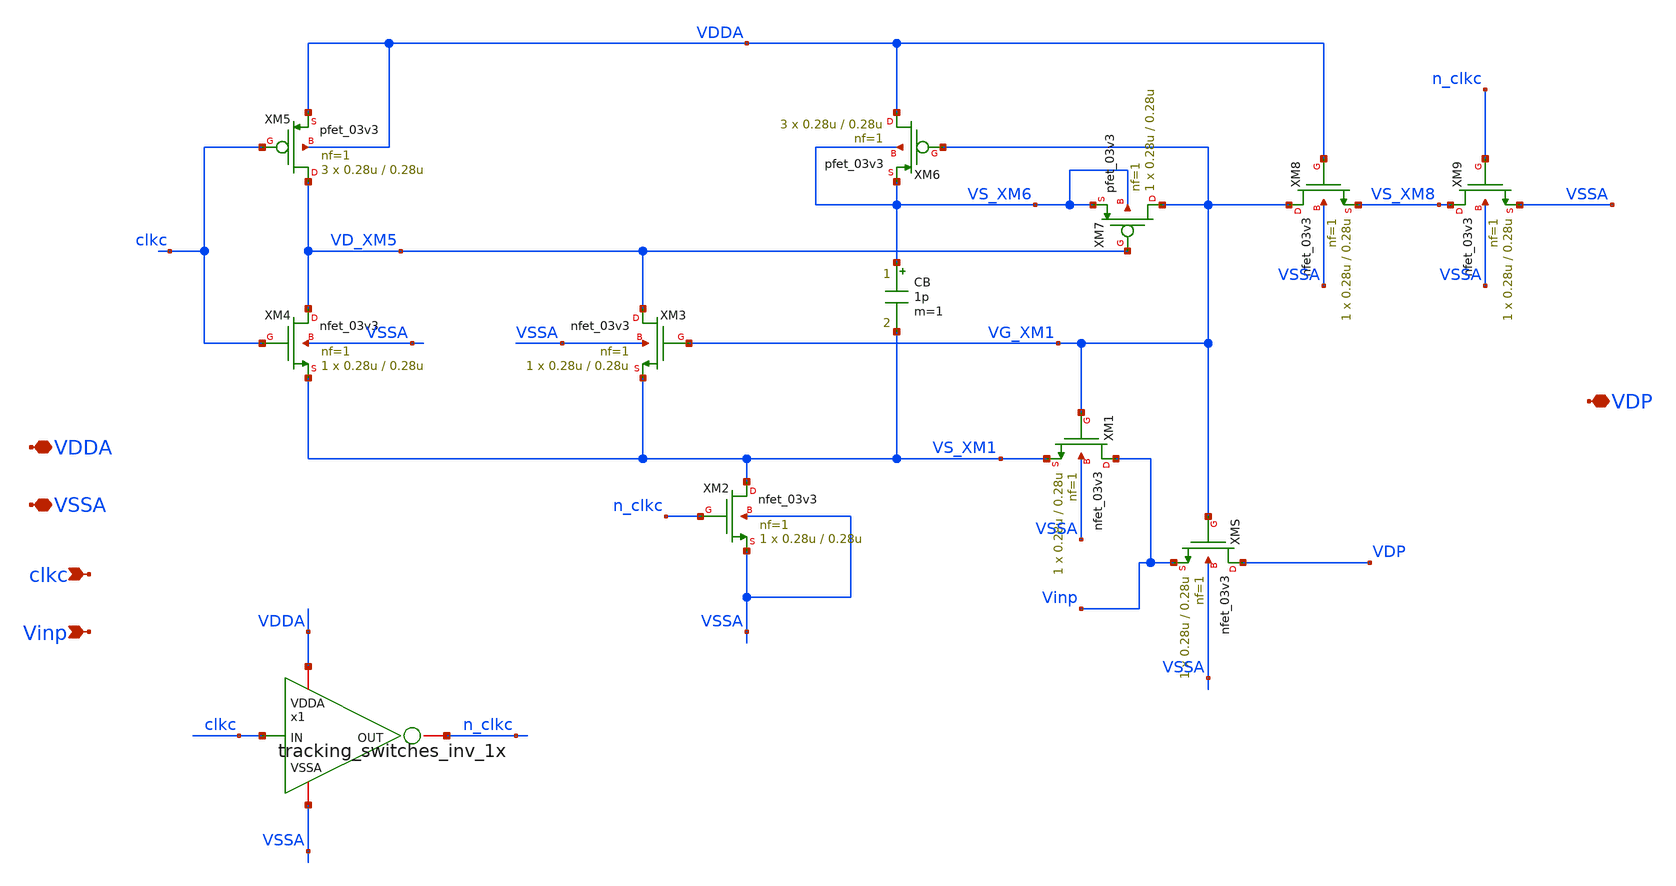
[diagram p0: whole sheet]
** sch_path: SAR_ADC/blocks/tracking_switches/tracking_switches.sch
**.subckt tracking_switches VDDA VSSA clkc Vinp VDP
*.iopin VDDA
*.iopin VSSA
*.ipin clkc
*.ipin Vinp
*.iopin VDP
XM2 VS_XM1 n_clkc VSSA VSSA nfet_03v3 L=0.28u W=0.28u nf=1 ad='int((nf+1)/2) * W/nf * 0.18u' as='int((nf+2)/2) * W/nf * 0.18u'
+ pd='2*int((nf+1)/2) * (W/nf + 0.18u)' ps='2*int((nf+2)/2) * (W/nf + 0.18u)' nrd='0.18u / W' nrs='0.18u / W'
+ sa=0 sb=0 sd=0 m=1
XM4 VD_XM5 clkc VS_XM1 VSSA nfet_03v3 L=0.28u W=0.28u nf=1 ad='int((nf+1)/2) * W/nf * 0.18u' as='int((nf+2)/2) * W/nf * 0.18u'
+ pd='2*int((nf+1)/2) * (W/nf + 0.18u)' ps='2*int((nf+2)/2) * (W/nf + 0.18u)' nrd='0.18u / W' nrs='0.18u / W'
+ sa=0 sb=0 sd=0 m=1
XM3 VD_XM5 VG_XM1 VS_XM1 VSSA nfet_03v3 L=0.28u W=0.28u nf=1 ad='int((nf+1)/2) * W/nf * 0.18u' as='int((nf+2)/2) * W/nf * 0.18u'
+ pd='2*int((nf+1)/2) * (W/nf + 0.18u)' ps='2*int((nf+2)/2) * (W/nf + 0.18u)' nrd='0.18u / W' nrs='0.18u / W'
+ sa=0 sb=0 sd=0 m=1
XM5 VD_XM5 clkc VDDA VDDA pfet_03v3 L=0.28u W=0.28u nf=1 ad='int((nf+1)/2) * W/nf * 0.18u' as='int((nf+2)/2) * W/nf * 0.18u'
+ pd='2*int((nf+1)/2) * (W/nf + 0.18u)' ps='2*int((nf+2)/2) * (W/nf + 0.18u)' nrd='0.18u / W' nrs='0.18u / W'
+ sa=0 sb=0 sd=0 m=3
XM6 VDDA VG_XM1 VS_XM6 VS_XM6 pfet_03v3 L=0.28u W=0.28u nf=1 ad='int((nf+1)/2) * W/nf * 0.18u' as='int((nf+2)/2) * W/nf * 0.18u'
+ pd='2*int((nf+1)/2) * (W/nf + 0.18u)' ps='2*int((nf+2)/2) * (W/nf + 0.18u)' nrd='0.18u / W' nrs='0.18u / W'
+ sa=0 sb=0 sd=0 m=3
CB VS_XM6 VS_XM1 1p m=1
XM7 VG_XM1 VD_XM5 VS_XM6 VS_XM6 pfet_03v3 L=0.28u W=0.28u nf=1 ad='int((nf+1)/2) * W/nf * 0.18u' as='int((nf+2)/2) * W/nf * 0.18u'
+ pd='2*int((nf+1)/2) * (W/nf + 0.18u)' ps='2*int((nf+2)/2) * (W/nf + 0.18u)' nrd='0.18u / W' nrs='0.18u / W'
+ sa=0 sb=0 sd=0 m=1
XM1 Vinp VG_XM1 VS_XM1 VSSA nfet_03v3 L=0.28u W=0.28u nf=1 ad='int((nf+1)/2) * W/nf * 0.18u' as='int((nf+2)/2) * W/nf * 0.18u'
+ pd='2*int((nf+1)/2) * (W/nf + 0.18u)' ps='2*int((nf+2)/2) * (W/nf + 0.18u)' nrd='0.18u / W' nrs='0.18u / W'
+ sa=0 sb=0 sd=0 m=1
XM9 VS_XM8 n_clkc VSSA VSSA nfet_03v3 L=0.28u W=0.28u nf=1 ad='int((nf+1)/2) * W/nf * 0.18u' as='int((nf+2)/2) * W/nf * 0.18u'
+ pd='2*int((nf+1)/2) * (W/nf + 0.18u)' ps='2*int((nf+2)/2) * (W/nf + 0.18u)' nrd='0.18u / W' nrs='0.18u / W'
+ sa=0 sb=0 sd=0 m=1
XM8 VG_XM1 VDDA VS_XM8 VSSA nfet_03v3 L=0.28u W=0.28u nf=1 ad='int((nf+1)/2) * W/nf * 0.18u' as='int((nf+2)/2) * W/nf * 0.18u'
+ pd='2*int((nf+1)/2) * (W/nf + 0.18u)' ps='2*int((nf+2)/2) * (W/nf + 0.18u)' nrd='0.18u / W' nrs='0.18u / W'
+ sa=0 sb=0 sd=0 m=1
XMS VDP VG_XM1 Vinp VSSA nfet_03v3 L=0.28u W=0.28u nf=1 ad='int((nf+1)/2) * W/nf * 0.18u' as='int((nf+2)/2) * W/nf * 0.18u'
+ pd='2*int((nf+1)/2) * (W/nf + 0.18u)' ps='2*int((nf+2)/2) * (W/nf + 0.18u)' nrd='0.18u / W' nrs='0.18u / W'
+ sa=0 sb=0 sd=0 m=1
x1 VDDA VSSA n_clkc clkc tracking_switches_inv_1x
**.ends

* expanding   symbol:
*+  /home/electrica/Documents/gf180_projects/gf180_work/PICO_contest/tracking_switches/tracking_switches_inv_1x.sym # of pins=4
** sym_path: SAR_ADC/blocks/tracking_switches/tracking_switches_inv_1x.sym
** sch_path: SAR_ADC/blocks/tracking_switches/tracking_switches_inv_1x.sch
.subckt tracking_switches_inv_1x VDDA VSSA OUT IN
*.iopin VDDA
*.iopin VSSA
*.iopin OUT
*.ipin IN
XM1 OUT IN VSSA VSSA nfet_03v3 L=0.28u W=0.22u nf=1 ad='int((nf+1)/2) * W/nf * 0.18u' as='int((nf+2)/2) * W/nf * 0.18u'
+ pd='2*int((nf+1)/2) * (W/nf + 0.18u)' ps='2*int((nf+2)/2) * (W/nf + 0.18u)' nrd='0.18u / W' nrs='0.18u / W'
+ sa=0 sb=0 sd=0 m=1
XM2 OUT IN VDDA VDDA pfet_03v3 L=0.28u W=0.66u nf=1 ad='int((nf+1)/2) * W/nf * 0.18u' as='int((nf+2)/2) * W/nf * 0.18u'
+ pd='2*int((nf+1)/2) * (W/nf + 0.18u)' ps='2*int((nf+2)/2) * (W/nf + 0.18u)' nrd='0.18u / W' nrs='0.18u / W'
+ sa=0 sb=0 sd=0 m=1
.ends

.end
